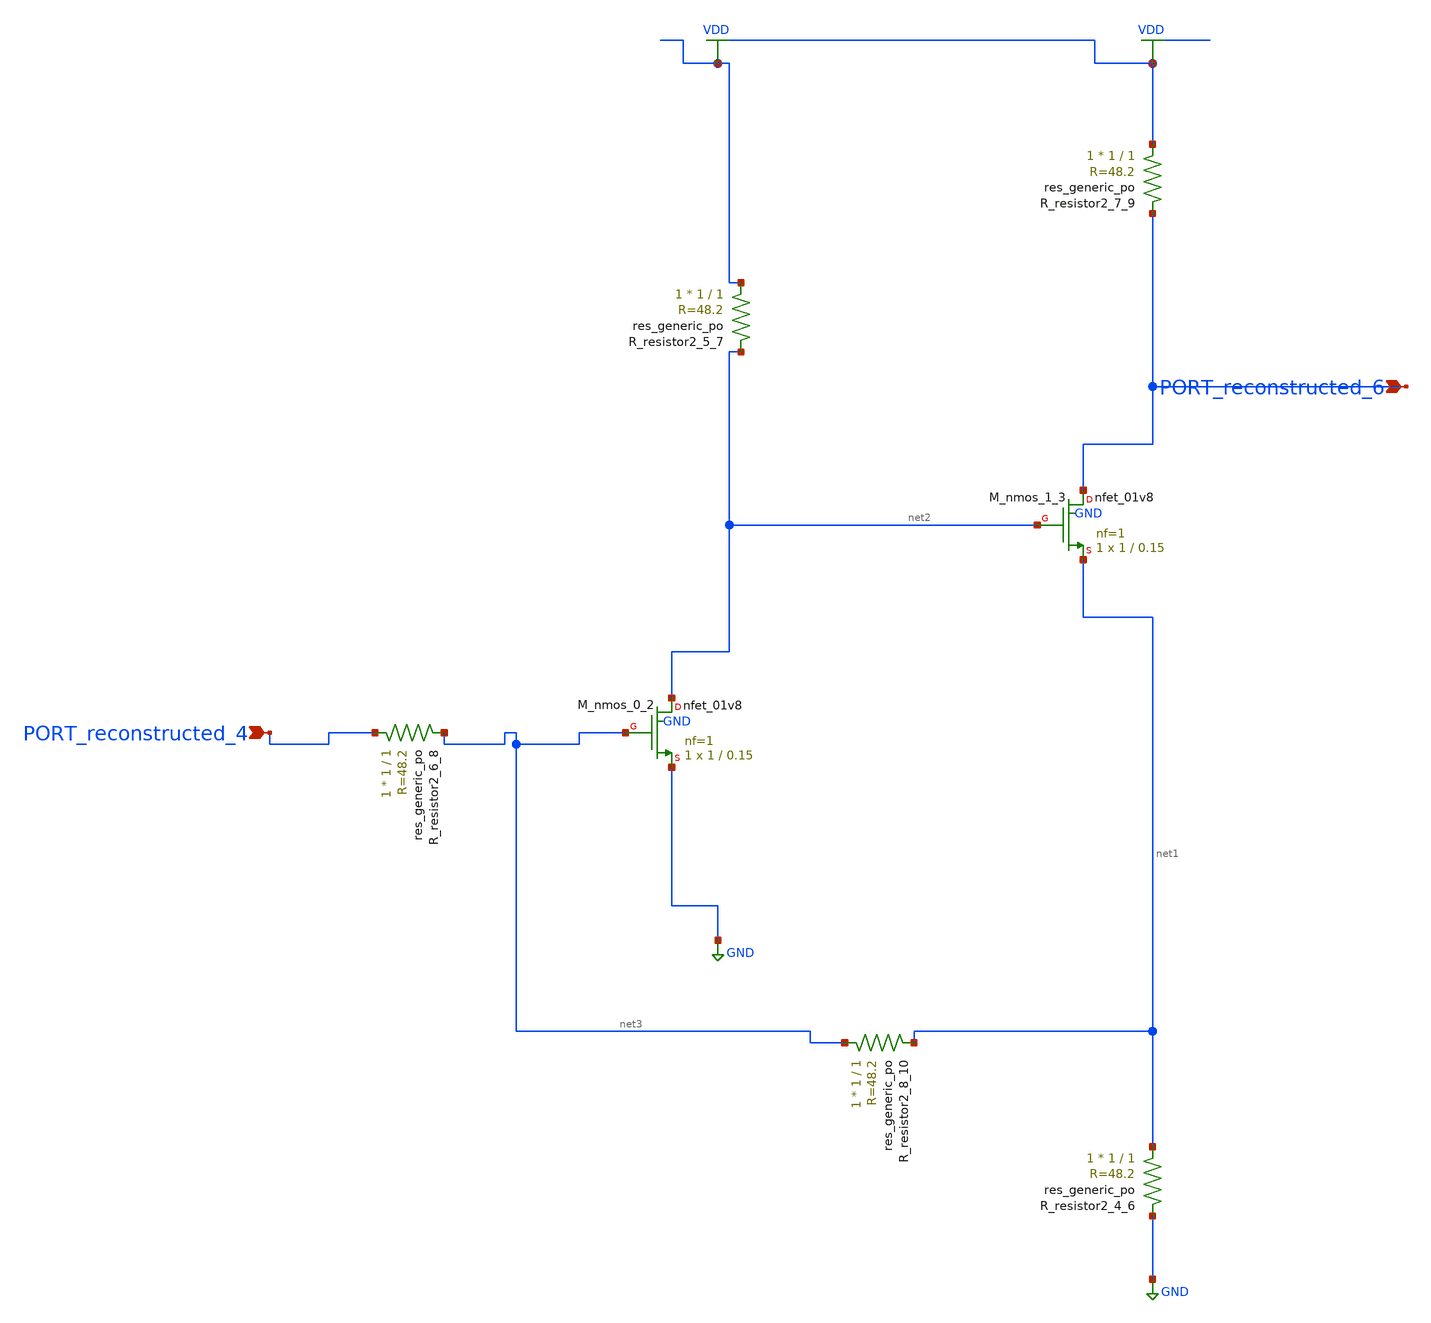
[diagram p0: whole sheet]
** sch_path: schematics/AMSNet/607.sch
**.subckt 607 PORT_reconstructed_6 PORT_reconstructed_4
*.ipin PORT_reconstructed_6
*.ipin PORT_reconstructed_4
XM_nmos_0_2 net2 net3 GND GND sky130_fd_pr__nfet_01v8 L=0.15 W=1 nf=1 ad='int((1 + 1)/2) * 1 / 1 * 0.29'
+ as='int((1 + 2)/2) * 1 / 1 * 0.29' pd='2*int((1 + 1)/2) * (1 / 1 + 0.29)' ps='2*int((1 + 2)/2) * (1 / 1 + 0.29)'
+ nrd='0.29 / 1 ' nrs='0.29 / 1 ' sa=0 sb=0 sd=0 mult=1 m=1
XM_nmos_1_3 PORT_reconstructed_6 net2 net1 GND sky130_fd_pr__nfet_01v8 L=0.15 W=1 nf=1 ad='int((1 + 1)/2) * 1 / 1 * 0.29'
+ as='int((1 + 2)/2) * 1 / 1 * 0.29' pd='2*int((1 + 1)/2) * (1 / 1 + 0.29)' ps='2*int((1 + 2)/2) * (1 / 1 + 0.29)'
+ nrd='0.29 / 1 ' nrs='0.29 / 1 ' sa=0 sb=0 sd=0 mult=1 m=1
XR_resistor2_4_6 net1 GND sky130_fd_pr__res_generic_po W=1 L=1 m=1
XR_resistor2_5_7 VDD net2 sky130_fd_pr__res_generic_po W=1 L=1 m=1
XR_resistor2_6_8 PORT_reconstructed_4 net3 sky130_fd_pr__res_generic_po W=1 L=1 m=1
XR_resistor2_7_9 VDD PORT_reconstructed_6 sky130_fd_pr__res_generic_po W=1 L=1 m=1
XR_resistor2_8_10 net3 net1 sky130_fd_pr__res_generic_po W=1 L=1 m=1
**.ends
.GLOBAL GND
.GLOBAL VDD
.end
